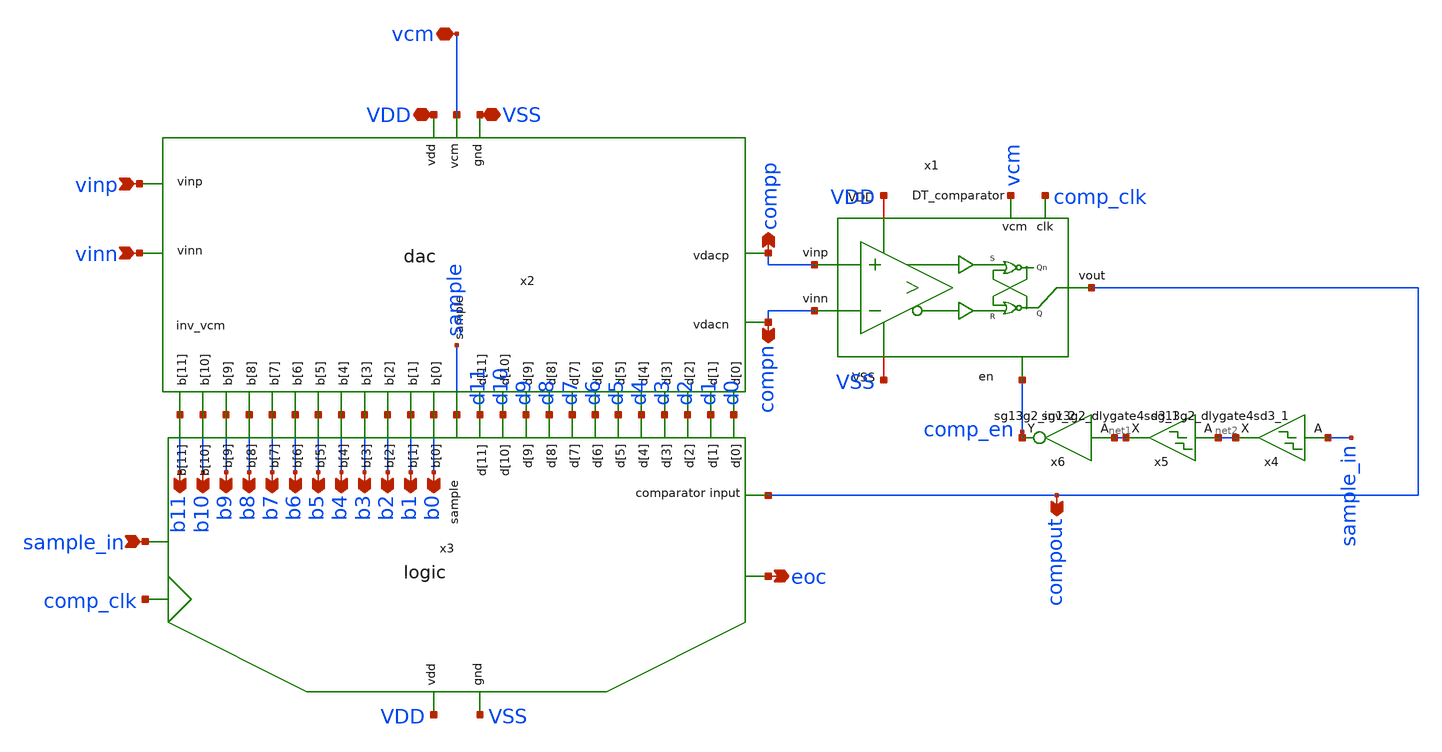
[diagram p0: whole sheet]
** sch_path: xschem/SAR_ADC/sar.sch
**.subckt sar vinp VDD b11 vinn VSS b10 b9 b8 b7 b6 b5 b4 b3 b2 b1 b0 compp compn compout eoc
*+ sample_in vcm
*.ipin vinp
*.iopin VDD
*.opin b11
*.ipin vinn
*.iopin VSS
*.opin b10
*.opin b9
*.opin b8
*.opin b7
*.opin b6
*.opin b5
*.opin b4
*.opin b3
*.opin b2
*.opin b1
*.opin b0
*.opin compp
*.opin compn
*.opin compout
*.opin eoc
*.ipin sample_in
*.iopin vcm
x1 VDD compp compout compn comp_en VSS comp_clk vcm DT_comparator
x2 compn vcm b9 b7 b0 b11 b3 b4 b2 b1 b8 b6 b5 b10 VSS VDD sample compp vinp vinn d9 d7 d0 d11 d3 d4
+ d2 d1 d8 d6 d5 d10 dac cu=10
x3 b9 b7 b0 b11 b3 b4 b2 b1 b8 b6 b5 b10 VSS VDD sample d9 d7 d0 d11 d3 d4 d2 d1 d8 d6 d5 d10
+ compout comp_clk sample_in eoc logic
x6 comp_en net1 VDD VSS sg13g2_inv_2
x5 net1 net2 VDD VSS sg13g2_dlygate4sd3_1
x4 net2 sample_in VDD VSS sg13g2_dlygate4sd3_1
**.ends
.end
